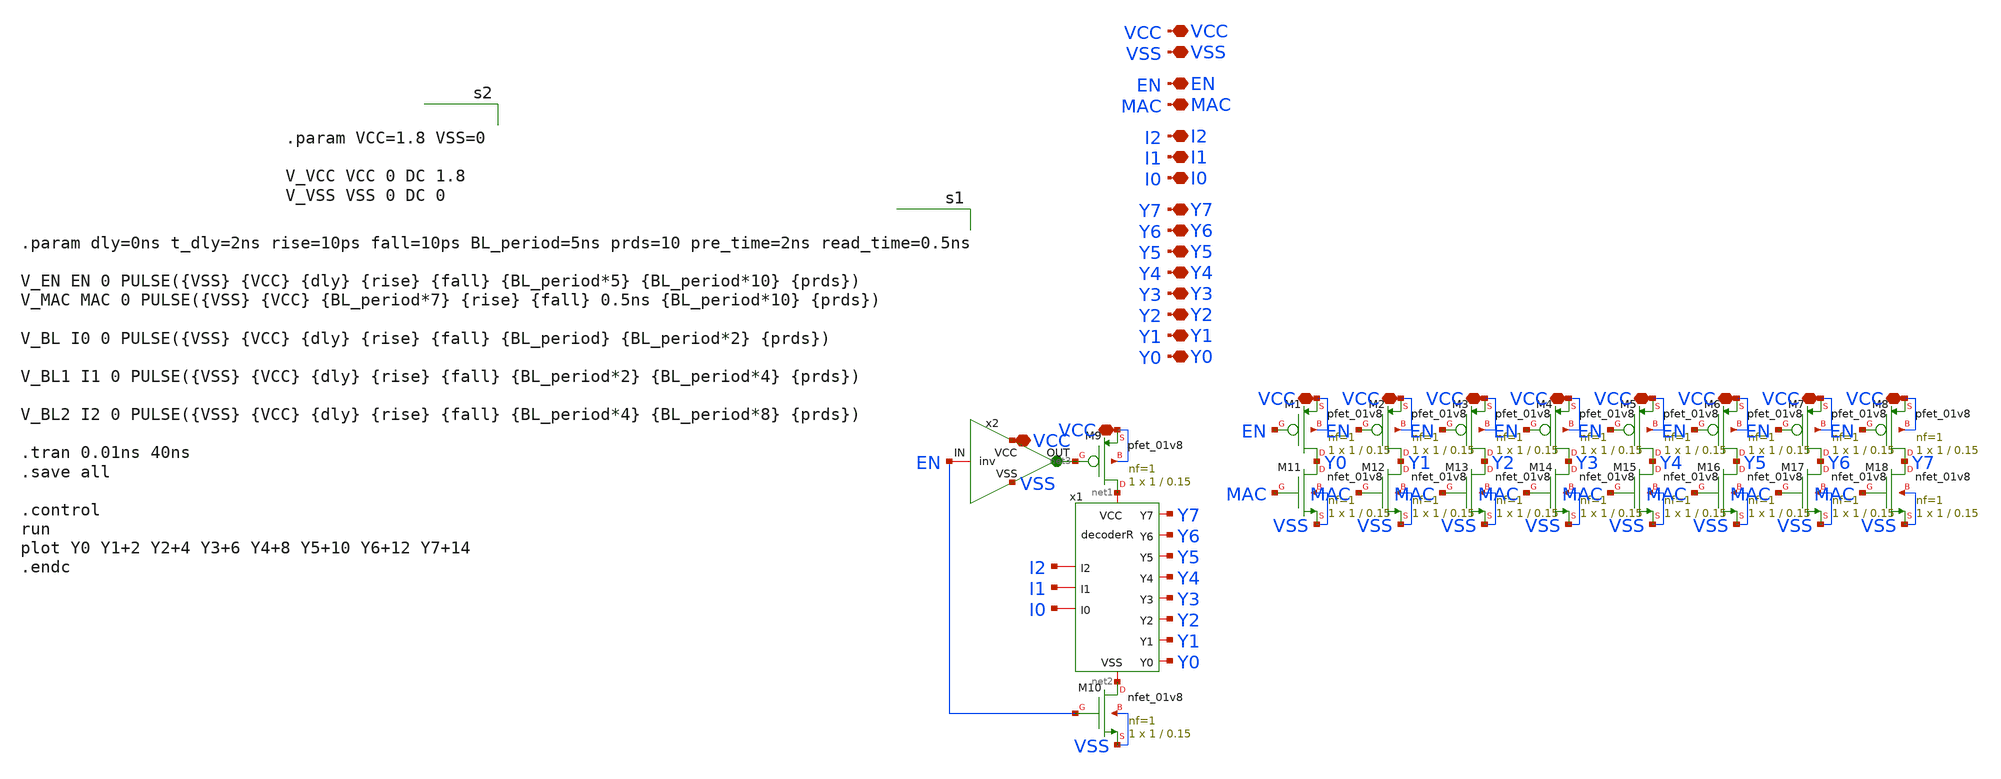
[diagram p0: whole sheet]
** sch_path: logic gates/decoderR_test.sch
**.subckt decoderR_test VCC VSS I2 I1 I0 Y7 Y6 Y5 Y4 Y3 Y2 Y1 Y0 VCC VCC VCC VCC VCC VCC VCC VCC EN
*+ VCC VCC MAC
*.iopin VCC
*.iopin VSS
*.iopin I2
*.iopin I1
*.iopin I0
*.iopin Y7
*.iopin Y6
*.iopin Y5
*.iopin Y4
*.iopin Y3
*.iopin Y2
*.iopin Y1
*.iopin Y0
*.iopin VCC
*.iopin VCC
*.iopin VCC
*.iopin VCC
*.iopin VCC
*.iopin VCC
*.iopin VCC
*.iopin VCC
*.iopin EN
*.iopin VCC
*.iopin VCC
*.iopin MAC
x1 net1 net2 I2 I1 I0 Y7 Y6 Y5 Y4 Y3 Y2 Y1 Y0 decoderR
XM1 Y0 EN VCC VCC sky130_fd_pr__pfet_01v8 L=0.15 W=1 nf=1 ad='int((nf+1)/2) * W/nf * 0.29' as='int((nf+2)/2) * W/nf * 0.29'
+ pd='2*int((nf+1)/2) * (W/nf + 0.29)' ps='2*int((nf+2)/2) * (W/nf + 0.29)' nrd='0.29 / W' nrs='0.29 / W'
+ sa=0 sb=0 sd=0 mult=1 m=1
XM2 Y1 EN VCC VCC sky130_fd_pr__pfet_01v8 L=0.15 W=1 nf=1 ad='int((nf+1)/2) * W/nf * 0.29' as='int((nf+2)/2) * W/nf * 0.29'
+ pd='2*int((nf+1)/2) * (W/nf + 0.29)' ps='2*int((nf+2)/2) * (W/nf + 0.29)' nrd='0.29 / W' nrs='0.29 / W'
+ sa=0 sb=0 sd=0 mult=1 m=1
XM3 Y2 EN VCC VCC sky130_fd_pr__pfet_01v8 L=0.15 W=1 nf=1 ad='int((nf+1)/2) * W/nf * 0.29' as='int((nf+2)/2) * W/nf * 0.29'
+ pd='2*int((nf+1)/2) * (W/nf + 0.29)' ps='2*int((nf+2)/2) * (W/nf + 0.29)' nrd='0.29 / W' nrs='0.29 / W'
+ sa=0 sb=0 sd=0 mult=1 m=1
XM4 Y3 EN VCC VCC sky130_fd_pr__pfet_01v8 L=0.15 W=1 nf=1 ad='int((nf+1)/2) * W/nf * 0.29' as='int((nf+2)/2) * W/nf * 0.29'
+ pd='2*int((nf+1)/2) * (W/nf + 0.29)' ps='2*int((nf+2)/2) * (W/nf + 0.29)' nrd='0.29 / W' nrs='0.29 / W'
+ sa=0 sb=0 sd=0 mult=1 m=1
XM5 Y4 EN VCC VCC sky130_fd_pr__pfet_01v8 L=0.15 W=1 nf=1 ad='int((nf+1)/2) * W/nf * 0.29' as='int((nf+2)/2) * W/nf * 0.29'
+ pd='2*int((nf+1)/2) * (W/nf + 0.29)' ps='2*int((nf+2)/2) * (W/nf + 0.29)' nrd='0.29 / W' nrs='0.29 / W'
+ sa=0 sb=0 sd=0 mult=1 m=1
XM6 Y5 EN VCC VCC sky130_fd_pr__pfet_01v8 L=0.15 W=1 nf=1 ad='int((nf+1)/2) * W/nf * 0.29' as='int((nf+2)/2) * W/nf * 0.29'
+ pd='2*int((nf+1)/2) * (W/nf + 0.29)' ps='2*int((nf+2)/2) * (W/nf + 0.29)' nrd='0.29 / W' nrs='0.29 / W'
+ sa=0 sb=0 sd=0 mult=1 m=1
XM7 Y6 EN VCC VCC sky130_fd_pr__pfet_01v8 L=0.15 W=1 nf=1 ad='int((nf+1)/2) * W/nf * 0.29' as='int((nf+2)/2) * W/nf * 0.29'
+ pd='2*int((nf+1)/2) * (W/nf + 0.29)' ps='2*int((nf+2)/2) * (W/nf + 0.29)' nrd='0.29 / W' nrs='0.29 / W'
+ sa=0 sb=0 sd=0 mult=1 m=1
XM8 Y7 EN VCC VCC sky130_fd_pr__pfet_01v8 L=0.15 W=1 nf=1 ad='int((nf+1)/2) * W/nf * 0.29' as='int((nf+2)/2) * W/nf * 0.29'
+ pd='2*int((nf+1)/2) * (W/nf + 0.29)' ps='2*int((nf+2)/2) * (W/nf + 0.29)' nrd='0.29 / W' nrs='0.29 / W'
+ sa=0 sb=0 sd=0 mult=1 m=1
XM9 net1 net3 VCC VCC sky130_fd_pr__pfet_01v8 L=0.15 W=1 nf=1 ad='int((nf+1)/2) * W/nf * 0.29' as='int((nf+2)/2) * W/nf * 0.29'
+ pd='2*int((nf+1)/2) * (W/nf + 0.29)' ps='2*int((nf+2)/2) * (W/nf + 0.29)' nrd='0.29 / W' nrs='0.29 / W'
+ sa=0 sb=0 sd=0 mult=1 m=1
x2 VCC EN net3 VSS inv
XM10 net2 EN VSS VSS sky130_fd_pr__nfet_01v8 L=0.15 W=1 nf=1 ad='int((1 + 1)/2) * 1 / 1 * 0.29' as='int((1 + 2)/2) * 1 / 1 * 0.29'
+ pd='2*int((1 + 1)/2) * (1 / 1 + 0.29)' ps='2*int((1 + 2)/2) * (1 / 1 + 0.29)' nrd='0.29 / 1 ' nrs='0.29 / 1 '
+ sa=0 sb=0 sd=0 mult=1 m=1
XM11 Y0 MAC VSS VSS sky130_fd_pr__nfet_01v8 L=0.15 W=1 nf=1 ad='int((1 + 1)/2) * 1 / 1 * 0.29' as='int((1 + 2)/2) * 1 / 1 * 0.29'
+ pd='2*int((1 + 1)/2) * (1 / 1 + 0.29)' ps='2*int((1 + 2)/2) * (1 / 1 + 0.29)' nrd='0.29 / 1 ' nrs='0.29 / 1 '
+ sa=0 sb=0 sd=0 mult=1 m=1
XM12 Y1 MAC VSS VSS sky130_fd_pr__nfet_01v8 L=0.15 W=1 nf=1 ad='int((1 + 1)/2) * 1 / 1 * 0.29' as='int((1 + 2)/2) * 1 / 1 * 0.29'
+ pd='2*int((1 + 1)/2) * (1 / 1 + 0.29)' ps='2*int((1 + 2)/2) * (1 / 1 + 0.29)' nrd='0.29 / 1 ' nrs='0.29 / 1 '
+ sa=0 sb=0 sd=0 mult=1 m=1
XM13 Y2 MAC VSS VSS sky130_fd_pr__nfet_01v8 L=0.15 W=1 nf=1 ad='int((1 + 1)/2) * 1 / 1 * 0.29' as='int((1 + 2)/2) * 1 / 1 * 0.29'
+ pd='2*int((1 + 1)/2) * (1 / 1 + 0.29)' ps='2*int((1 + 2)/2) * (1 / 1 + 0.29)' nrd='0.29 / 1 ' nrs='0.29 / 1 '
+ sa=0 sb=0 sd=0 mult=1 m=1
XM14 Y3 MAC VSS VSS sky130_fd_pr__nfet_01v8 L=0.15 W=1 nf=1 ad='int((1 + 1)/2) * 1 / 1 * 0.29' as='int((1 + 2)/2) * 1 / 1 * 0.29'
+ pd='2*int((1 + 1)/2) * (1 / 1 + 0.29)' ps='2*int((1 + 2)/2) * (1 / 1 + 0.29)' nrd='0.29 / 1 ' nrs='0.29 / 1 '
+ sa=0 sb=0 sd=0 mult=1 m=1
XM15 Y4 MAC VSS VSS sky130_fd_pr__nfet_01v8 L=0.15 W=1 nf=1 ad='int((1 + 1)/2) * 1 / 1 * 0.29' as='int((1 + 2)/2) * 1 / 1 * 0.29'
+ pd='2*int((1 + 1)/2) * (1 / 1 + 0.29)' ps='2*int((1 + 2)/2) * (1 / 1 + 0.29)' nrd='0.29 / 1 ' nrs='0.29 / 1 '
+ sa=0 sb=0 sd=0 mult=1 m=1
XM16 Y5 MAC VSS VSS sky130_fd_pr__nfet_01v8 L=0.15 W=1 nf=1 ad='int((1 + 1)/2) * 1 / 1 * 0.29' as='int((1 + 2)/2) * 1 / 1 * 0.29'
+ pd='2*int((1 + 1)/2) * (1 / 1 + 0.29)' ps='2*int((1 + 2)/2) * (1 / 1 + 0.29)' nrd='0.29 / 1 ' nrs='0.29 / 1 '
+ sa=0 sb=0 sd=0 mult=1 m=1
XM17 Y6 MAC VSS VSS sky130_fd_pr__nfet_01v8 L=0.15 W=1 nf=1 ad='int((1 + 1)/2) * 1 / 1 * 0.29' as='int((1 + 2)/2) * 1 / 1 * 0.29'
+ pd='2*int((1 + 1)/2) * (1 / 1 + 0.29)' ps='2*int((1 + 2)/2) * (1 / 1 + 0.29)' nrd='0.29 / 1 ' nrs='0.29 / 1 '
+ sa=0 sb=0 sd=0 mult=1 m=1
XM18 Y7 MAC VSS VSS sky130_fd_pr__nfet_01v8 L=0.15 W=1 nf=1 ad='int((1 + 1)/2) * 1 / 1 * 0.29' as='int((1 + 2)/2) * 1 / 1 * 0.29'
+ pd='2*int((1 + 1)/2) * (1 / 1 + 0.29)' ps='2*int((1 + 2)/2) * (1 / 1 + 0.29)' nrd='0.29 / 1 ' nrs='0.29 / 1 '
+ sa=0 sb=0 sd=0 mult=1 m=1
**** begin user architecture code


.param dly=0ns t_dly=2ns rise=10ps fall=10ps BL_period=5ns prds=10 pre_time=2ns read_time=0.5ns

V_EN EN 0 PULSE({VSS} {VCC} {dly} {rise} {fall} {BL_period*5} {BL_period*10} {prds})
V_MAC MAC 0 PULSE({VSS} {VCC} {BL_period*7} {rise} {fall} 0.5ns {BL_period*10} {prds})

V_BL I0 0 PULSE({VSS} {VCC} {dly} {rise} {fall} {BL_period} {BL_period*2} {prds})

V_BL1 I1 0 PULSE({VSS} {VCC} {dly} {rise} {fall} {BL_period*2} {BL_period*4} {prds})

V_BL2 I2 0 PULSE({VSS} {VCC} {dly} {rise} {fall} {BL_period*4} {BL_period*8} {prds})

.tran 0.01ns 40ns
.save all

.control
run
plot Y0 Y1+2 Y2+4 Y3+6 Y4+8 Y5+10 Y6+12 Y7+14
.endc



** opencircuitdesign pdks install
.lib $::SKYWATER_MODELS/sky130.lib.spice tt



.param VCC=1.8 VSS=0

V_VCC VCC 0 DC 1.8
V_VSS VSS 0 DC 0


**** end user architecture code
**.ends

* expanding   symbol:  logic gates/decoderR.sym # of pins=13
** sym_path: logic gates/decoderR.sym
** sch_path: logic gates/decoderR.sch
.subckt decoderR VCC VSS I2 I1 I0 Y7 Y6 Y5 Y4 Y3 Y2 Y1 Y0
*.iopin I2
*.iopin I1
*.iopin I0
*.iopin Y7
*.iopin Y6
*.iopin Y5
*.iopin Y4
*.iopin Y3
*.iopin Y2
*.iopin Y1
*.iopin Y0
*.iopin VCC
*.iopin VSS
x3 VCC I2 net3 VSS inv
x4 VCC I1 net2 VSS inv
x5 VCC I0 net1 VSS inv
x1 VCC Y7 I2 I1 I0 VSS nand3
x2 VCC Y6 I2 I1 net1 VSS nand3
x6 VCC Y5 I2 net2 I0 VSS nand3
x7 VCC Y4 I2 net2 net1 VSS nand3
x8 VCC Y3 net3 I1 I0 VSS nand3
x9 VCC Y2 net3 I1 net1 VSS nand3
x10 VCC Y1 net3 net2 I0 VSS nand3
x11 VCC Y0 net3 net2 net1 VSS nand3
.ends


* expanding   symbol:  inv.sym # of pins=4
** sym_path: logic gates/inv.sym
** sch_path: logic gates/inv.sch
.subckt inv VCC IN OUT VSS
*.iopin VCC
*.iopin IN
*.iopin OUT
*.iopin VSS
XM1 OUT IN VSS VSS sky130_fd_pr__nfet_01v8 L=0.15 W=0.5 nf=1 ad='int((nf+1)/2) * W/nf * 0.29' as='int((nf+2)/2) * W/nf * 0.29'
+ pd='2*int((nf+1)/2) * (W/nf + 0.29)' ps='2*int((nf+2)/2) * (W/nf + 0.29)' nrd='0.29 / W' nrs='0.29 / W'
+ sa=0 sb=0 sd=0 mult=1 m=1
XM2 OUT IN VCC VCC sky130_fd_pr__pfet_01v8 L=0.15 W=1.05 nf=1 ad='int((nf+1)/2) * W/nf * 0.29' as='int((nf+2)/2) * W/nf * 0.29'
+ pd='2*int((nf+1)/2) * (W/nf + 0.29)' ps='2*int((nf+2)/2) * (W/nf + 0.29)' nrd='0.29 / W' nrs='0.29 / W'
+ sa=0 sb=0 sd=0 mult=1 m=1
.ends


* expanding   symbol:  logic gates/nand3.sym # of pins=6
** sym_path: logic gates/nand3.sym
** sch_path: logic gates/nand3.sch
.subckt nand3 VCC Y A B C VSS
*.iopin VCC
*.iopin VSS
*.iopin Y
*.iopin A
*.iopin B
*.iopin C
XM2 net1 C VSS VSS sky130_fd_pr__nfet_01v8 L=0.15 W=1 nf=1 ad='int((1 + 1)/2) * 1 / 1 * 0.29' as='int((1 + 2)/2) * 1 / 1 * 0.29'
+ pd='2*int((1 + 1)/2) * (1 / 1 + 0.29)' ps='2*int((1 + 2)/2) * (1 / 1 + 0.29)' nrd='0.29 / 1 ' nrs='0.29 / 1 '
+ sa=0 sb=0 sd=0 mult=1 m=1
XM11 Y A VCC VCC sky130_fd_pr__pfet_01v8 L=0.15 W=1 nf=1 ad='int((nf+1)/2) * W/nf * 0.29' as='int((nf+2)/2) * W/nf * 0.29'
+ pd='2*int((nf+1)/2) * (W/nf + 0.29)' ps='2*int((nf+2)/2) * (W/nf + 0.29)' nrd='0.29 / W' nrs='0.29 / W'
+ sa=0 sb=0 sd=0 mult=1 m=1
XM1 Y A net2 VSS sky130_fd_pr__nfet_01v8 L=0.15 W=1 nf=1 ad='int((1 + 1)/2) * 1 / 1 * 0.29' as='int((1 + 2)/2) * 1 / 1 * 0.29'
+ pd='2*int((1 + 1)/2) * (1 / 1 + 0.29)' ps='2*int((1 + 2)/2) * (1 / 1 + 0.29)' nrd='0.29 / 1 ' nrs='0.29 / 1 '
+ sa=0 sb=0 sd=0 mult=1 m=1
XM3 Y B VCC VCC sky130_fd_pr__pfet_01v8 L=0.15 W=1 nf=1 ad='int((nf+1)/2) * W/nf * 0.29' as='int((nf+2)/2) * W/nf * 0.29'
+ pd='2*int((nf+1)/2) * (W/nf + 0.29)' ps='2*int((nf+2)/2) * (W/nf + 0.29)' nrd='0.29 / W' nrs='0.29 / W'
+ sa=0 sb=0 sd=0 mult=1 m=1
XM4 Y C VCC VCC sky130_fd_pr__pfet_01v8 L=0.15 W=1 nf=1 ad='int((nf+1)/2) * W/nf * 0.29' as='int((nf+2)/2) * W/nf * 0.29'
+ pd='2*int((nf+1)/2) * (W/nf + 0.29)' ps='2*int((nf+2)/2) * (W/nf + 0.29)' nrd='0.29 / W' nrs='0.29 / W'
+ sa=0 sb=0 sd=0 mult=1 m=1
XM5 net2 B net1 VSS sky130_fd_pr__nfet_01v8 L=0.15 W=1 nf=1 ad='int((1 + 1)/2) * 1 / 1 * 0.29' as='int((1 + 2)/2) * 1 / 1 * 0.29'
+ pd='2*int((1 + 1)/2) * (1 / 1 + 0.29)' ps='2*int((1 + 2)/2) * (1 / 1 + 0.29)' nrd='0.29 / 1 ' nrs='0.29 / 1 '
+ sa=0 sb=0 sd=0 mult=1 m=1
.ends

.end
